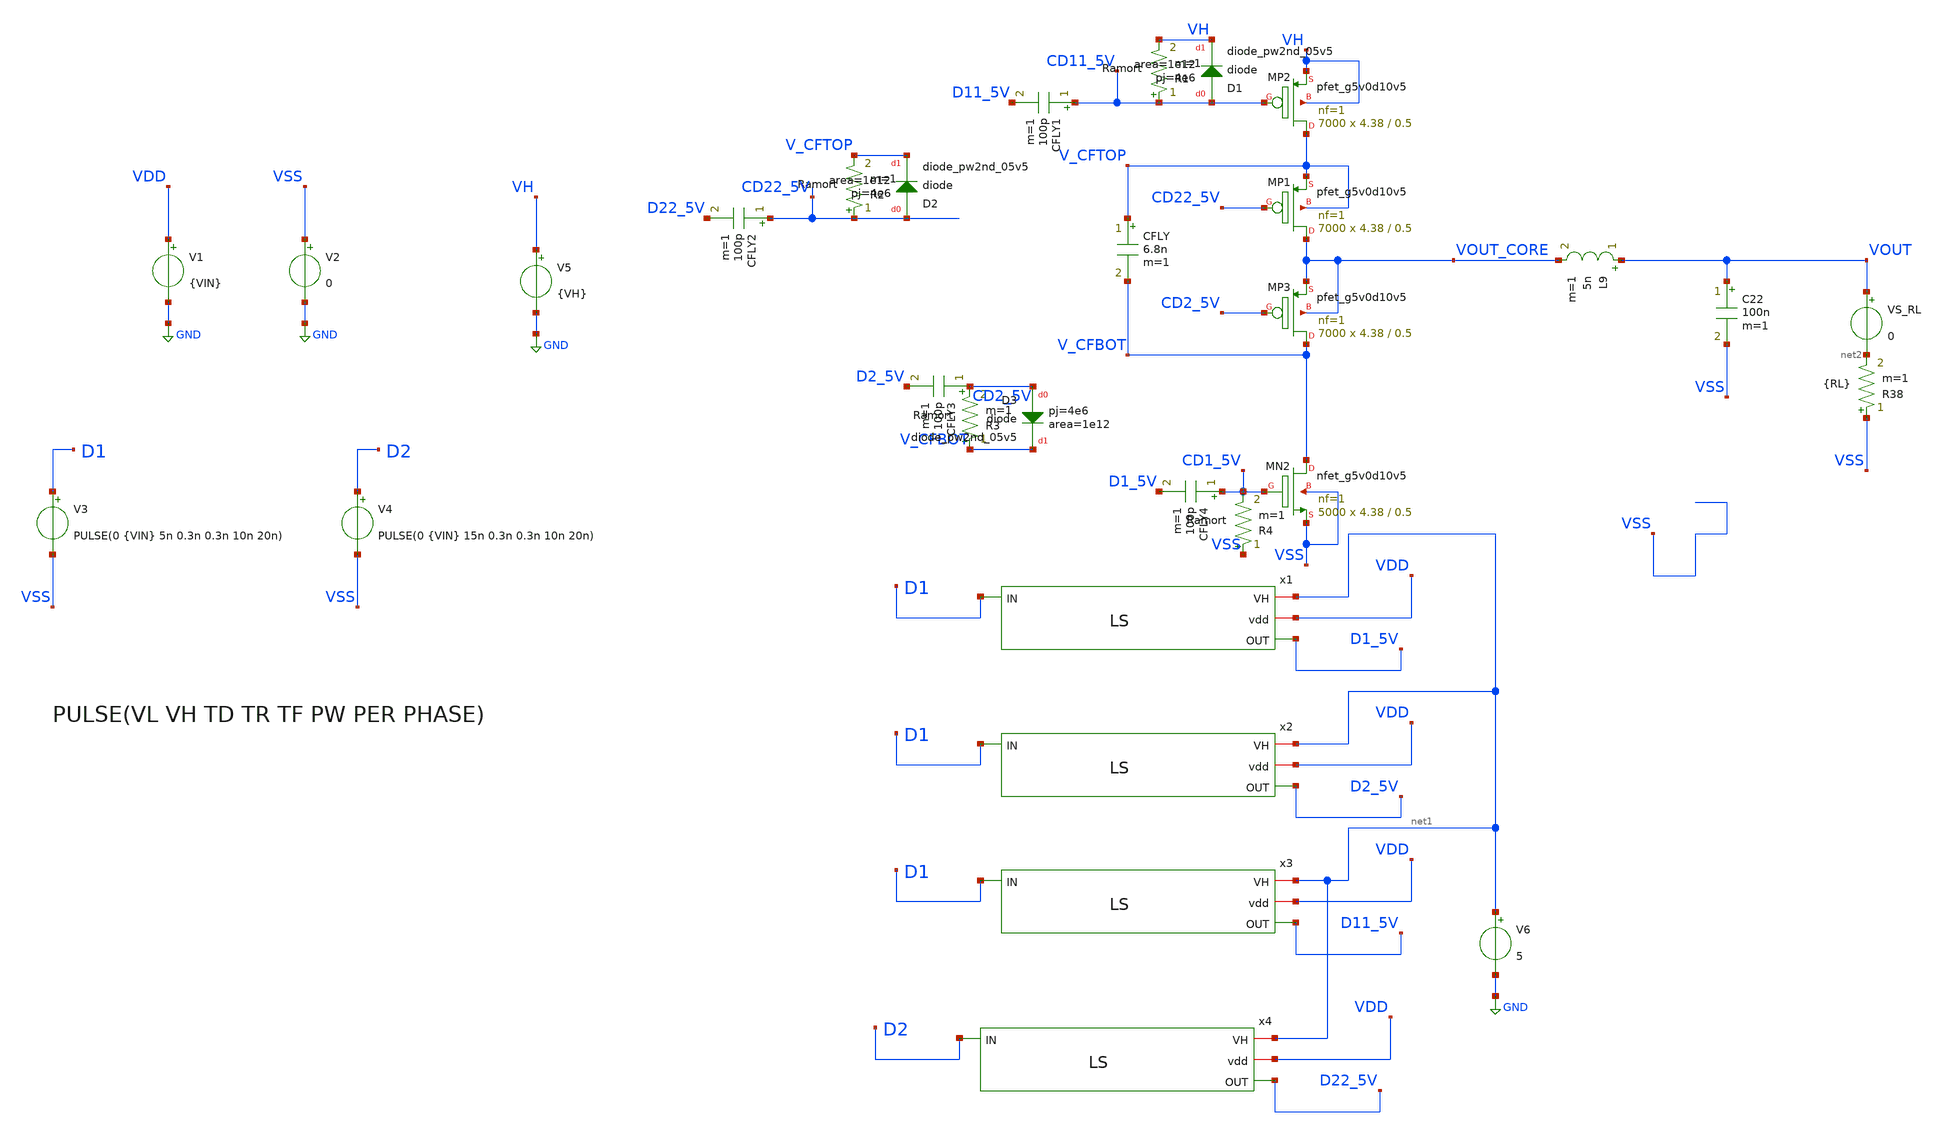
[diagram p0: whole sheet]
** sch_path: xschem/dev_switches/DCDC_10V/DCDC_v1p3_100MHz_NMOS_PMOS_Z_jm.sch
**.subckt DCDC_v1p3_100MHz_NMOS_PMOS_Z_jm
CFLY V_CFTOP V_CFBOT 6.8n m=1
V1 VDD GND {VIN}
V3 D1 VSS PULSE(0 {VIN} 5n 0.3n 0.3n 10n 20n)
V2 VSS GND 0
V4 D2 VSS PULSE(0 {VIN} 15n 0.3n 0.3n 10n 20n)
L9 VOUT VOUT_CORE 5n m=1
C22 VOUT VSS 100n m=1
R38 VSS net2 {RL} m=1
VS_RL VOUT net2 0
x1 net1 VDD D1_5V D1 LS
V5 VH GND {VH}
x2 net1 VDD D2_5V D1 LS
XMP2 V_CFTOP CD11_5V VH VH sky130_fd_pr__pfet_g5v0d10v5 L=0.5 W=4.38 nf=1 ad='int((nf+1)/2) * W/nf * 0.29'
+ as='int((nf+2)/2) * W/nf * 0.29' pd='2*int((nf+1)/2) * (W/nf + 0.29)' ps='2*int((nf+2)/2) * (W/nf + 0.29)'
+ nrd='0.29 / W' nrs='0.29 / W' sa=0 sb=0 sd=0 mult=7000 m=7000
XMP1 VOUT_CORE CD22_5V V_CFTOP V_CFTOP sky130_fd_pr__pfet_g5v0d10v5 L=0.5 W=4.38 nf=1 ad='int((nf+1)/2) * W/nf * 0.29'
+ as='int((nf+2)/2) * W/nf * 0.29' pd='2*int((nf+1)/2) * (W/nf + 0.29)' ps='2*int((nf+2)/2) * (W/nf + 0.29)'
+ nrd='0.29 / W' nrs='0.29 / W' sa=0 sb=0 sd=0 mult=7000 m=7000
CFLY1 CD11_5V D11_5V 100p m=1
XD1 CD11_5V VH sky130_fd_pr__diode_pw2nd_05v5 area=1e12 pj=4e6
x3 net1 VDD D11_5V D1 LS
R1 CD11_5V VH Ramort m=1
V6 net1 GND 5
CFLY2 CD22_5V D22_5V 100p m=1
XD2 CD22_5V V_CFTOP sky130_fd_pr__diode_pw2nd_05v5 area=1e12 pj=4e6
R2 CD22_5V V_CFTOP Ramort m=1
x4 net1 VDD D22_5V D2 LS
R3 V_CFBOT CD2_5V Ramort m=1
CFLY3 CD2_5V D2_5V 100p m=1
XMP3 V_CFBOT CD2_5V VOUT_CORE VOUT_CORE sky130_fd_pr__pfet_g5v0d10v5 L=0.5 W=4.38 nf=1 ad='int((nf+1)/2) * W/nf * 0.29'
+ as='int((nf+2)/2) * W/nf * 0.29' pd='2*int((nf+1)/2) * (W/nf + 0.29)' ps='2*int((nf+2)/2) * (W/nf + 0.29)'
+ nrd='0.29 / W' nrs='0.29 / W' sa=0 sb=0 sd=0 mult=7000 m=7000
XD3 CD2_5V V_CFBOT sky130_fd_pr__diode_pw2nd_05v5 area=1e12 pj=4e6
XMN2 V_CFBOT CD1_5V VSS VSS sky130_fd_pr__nfet_g5v0d10v5 L=0.5 W=4.38 nf=1 ad='int((nf+1)/2) * W/nf * 0.29'
+ as='int((nf+2)/2) * W/nf * 0.29' pd='2*int((nf+1)/2) * (W/nf + 0.29)' ps='2*int((nf+2)/2) * (W/nf + 0.29)'
+ nrd='0.29 / W' nrs='0.29 / W' sa=0 sb=0 sd=0 mult=5000 m=5000
CFLY4 CD1_5V D1_5V 100p m=1
R4 VSS CD1_5V Ramort m=1
**** begin user architecture code


.param VIN = 1.8
.param VH = 10
.param RL = 500
.param Ramort=1k
.option scale=1e-6
*.option temp=70
.ic v(V_CFTOP) = VIN/2
.ic v(vout)=0
.ic v(V_CFBOT) = 0
.probe vd(MP2:G:S)

.param mc_mm_switch=0
*.lib /usr/share/pdk/sky130A/libs.tech/ngspice/sky130.lib.spice tt
*.lib /foss/pdk/sky130A/libs.tech/ngspice/sky130.lib.spice TT
.lib /home/jorge/Documents/Postdoc/share/pdk/sky130A/libs.tech/ngspice/sky130.lib.spice tt
*.include /usr/share/pdk/sky130A/libs.ref/sky130_fd_sc_hvl/spice/sky130_fd_sc_hvl.spice
*.include /home/jorge/Documents/Postdoc/share/pdk/sky130A/libs.ref/sky130_fd_sc_hvl/spice/sky130_fd_sc_hvl.spice
.options savecurrents
.control
save all
tran 1n 2u
write DCDC_v1p3_100MHz_NMOS_PMOS_Z_jm.raw
foreach barrido 1k 2k 3k 4k 5k
alterparam Ramort = $barrido
.endc


**** end user architecture code
**.ends
.GLOBAL GND
.end
